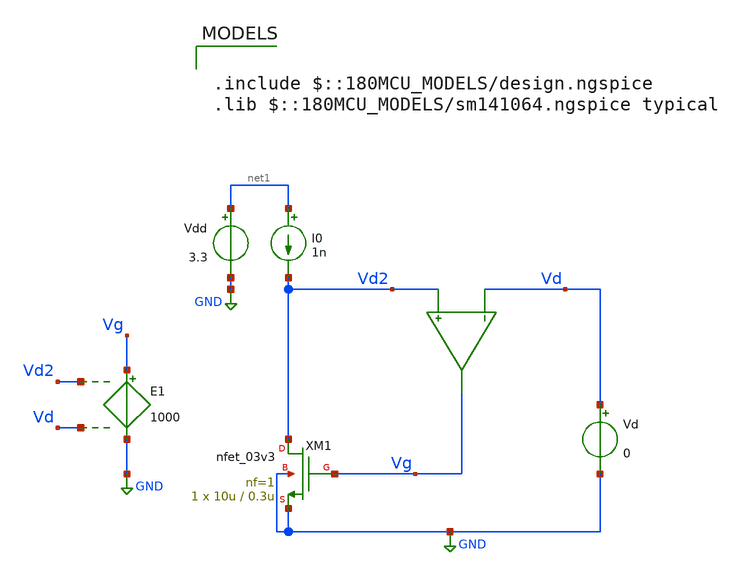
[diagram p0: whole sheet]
** sch_path: legacy/Examples/GF180MCU/xschem/Extraction/nmos_sigma_ext.sch
**.subckt nmos_sigma_ext
I0 net1 Vd2 1n
Vd Vd GND 0
Vdd net1 GND 3.3
E1 Vg GND Vd2 Vd 1000
XM1 Vd2 Vg GND GND nfet_03v3 L=0.3u W=10u nf=1 ad='int((nf+1)/2) * W/nf * 0.18u' as='int((nf+2)/2) * W/nf * 0.18u'
+ pd='2*int((nf+1)/2) * (W/nf + 0.18u)' ps='2*int((nf+2)/2) * (W/nf + 0.18u)' nrd='0.18u / W' nrs='0.18u / W'
+ sa=0 sb=0 sd=0 m=1
**** begin user architecture code

.include $::180MCU_MODELS/design.ngspice
.lib $::180MCU_MODELS/sm141064.ngspice typical




.control
save all

dc Vd 0.2 3.5 25.9m

let vd_interp = 3.3/3
let sigma = -deriv(V(vg))/deriv(V(vd))
save sigma

echo
echo
echo


echo Sigma @ VD=$&vd_interp:
meas dc sigma_value FIND sigma WHEN V(vd)=vd_interp

echo
echo
echo
write nmos_sigma_ext.raw

.endc




**** end user architecture code
**.ends
.GLOBAL GND
.end
